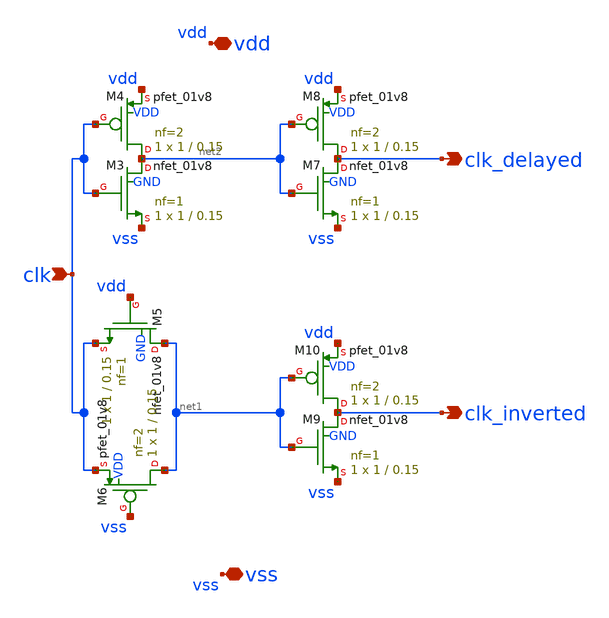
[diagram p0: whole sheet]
** sch_path: xschem/clock_phases.sch
**.subckt clock_phases clk vdd clk_delayed clk_inverted vss
*.ipin clk
*.iopin vdd
*.opin clk_delayed
*.opin clk_inverted
*.iopin vss
XM3 net2 clk vss GND sky130_fd_pr__nfet_01v8 L=0.15 W=1 nf=1 ad='int((nf+1)/2) * W/nf * 0.29' as='int((nf+2)/2) * W/nf * 0.29'
+ pd='2*int((nf+1)/2) * (W/nf + 0.29)' ps='2*int((nf+2)/2) * (W/nf + 0.29)' nrd='0.29 / W' nrs='0.29 / W'
+ sa=0 sb=0 sd=0 mult=1 m=1
XM4 net2 clk vdd VDD sky130_fd_pr__pfet_01v8 L=0.15 W=1 nf=2 ad='int((nf+1)/2) * W/nf * 0.29' as='int((nf+2)/2) * W/nf * 0.29'
+ pd='2*int((nf+1)/2) * (W/nf + 0.29)' ps='2*int((nf+2)/2) * (W/nf + 0.29)' nrd='0.29 / W' nrs='0.29 / W'
+ sa=0 sb=0 sd=0 mult=1 m=1
XM5 net1 vdd clk GND sky130_fd_pr__nfet_01v8 L=0.15 W=1 nf=1 ad='int((nf+1)/2) * W/nf * 0.29' as='int((nf+2)/2) * W/nf * 0.29'
+ pd='2*int((nf+1)/2) * (W/nf + 0.29)' ps='2*int((nf+2)/2) * (W/nf + 0.29)' nrd='0.29 / W' nrs='0.29 / W'
+ sa=0 sb=0 sd=0 mult=1 m=1
XM6 net1 vss clk VDD sky130_fd_pr__pfet_01v8 L=0.15 W=1 nf=2 ad='int((nf+1)/2) * W/nf * 0.29' as='int((nf+2)/2) * W/nf * 0.29'
+ pd='2*int((nf+1)/2) * (W/nf + 0.29)' ps='2*int((nf+2)/2) * (W/nf + 0.29)' nrd='0.29 / W' nrs='0.29 / W'
+ sa=0 sb=0 sd=0 mult=1 m=1
XM7 clk_delayed net2 vss GND sky130_fd_pr__nfet_01v8 L=0.15 W=1 nf=1 ad='int((nf+1)/2) * W/nf * 0.29'
+ as='int((nf+2)/2) * W/nf * 0.29' pd='2*int((nf+1)/2) * (W/nf + 0.29)' ps='2*int((nf+2)/2) * (W/nf + 0.29)'
+ nrd='0.29 / W' nrs='0.29 / W' sa=0 sb=0 sd=0 mult=1 m=1
XM8 clk_delayed net2 vdd VDD sky130_fd_pr__pfet_01v8 L=0.15 W=1 nf=2 ad='int((nf+1)/2) * W/nf * 0.29'
+ as='int((nf+2)/2) * W/nf * 0.29' pd='2*int((nf+1)/2) * (W/nf + 0.29)' ps='2*int((nf+2)/2) * (W/nf + 0.29)'
+ nrd='0.29 / W' nrs='0.29 / W' sa=0 sb=0 sd=0 mult=1 m=1
XM9 clk_inverted net1 vss GND sky130_fd_pr__nfet_01v8 L=0.15 W=1 nf=1 ad='int((nf+1)/2) * W/nf * 0.29'
+ as='int((nf+2)/2) * W/nf * 0.29' pd='2*int((nf+1)/2) * (W/nf + 0.29)' ps='2*int((nf+2)/2) * (W/nf + 0.29)'
+ nrd='0.29 / W' nrs='0.29 / W' sa=0 sb=0 sd=0 mult=1 m=1
XM10 clk_inverted net1 vdd VDD sky130_fd_pr__pfet_01v8 L=0.15 W=1 nf=2 ad='int((nf+1)/2) * W/nf * 0.29'
+ as='int((nf+2)/2) * W/nf * 0.29' pd='2*int((nf+1)/2) * (W/nf + 0.29)' ps='2*int((nf+2)/2) * (W/nf + 0.29)'
+ nrd='0.29 / W' nrs='0.29 / W' sa=0 sb=0 sd=0 mult=1 m=1
**.ends
.end
